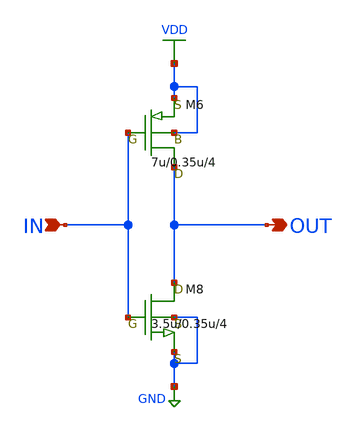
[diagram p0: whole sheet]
** sch_path: LR_hasegawa/LR_Work2/symbol/INVERTER.sch
**.subckt INVERTER OUT IN
*.opin OUT
*.ipin IN
M6 OUT IN VDD VDD pch w=7u l=0.35u as=5.6p ps=9u ad=5.6p pd=9u m=4
M8 OUT IN GND GND nch w=3.5u l=0.35u as=2.8p ps=5.5u ad=2.8p pd=5.5u m=4
**.ends
.GLOBAL VDD
.GLOBAL GND
.end
